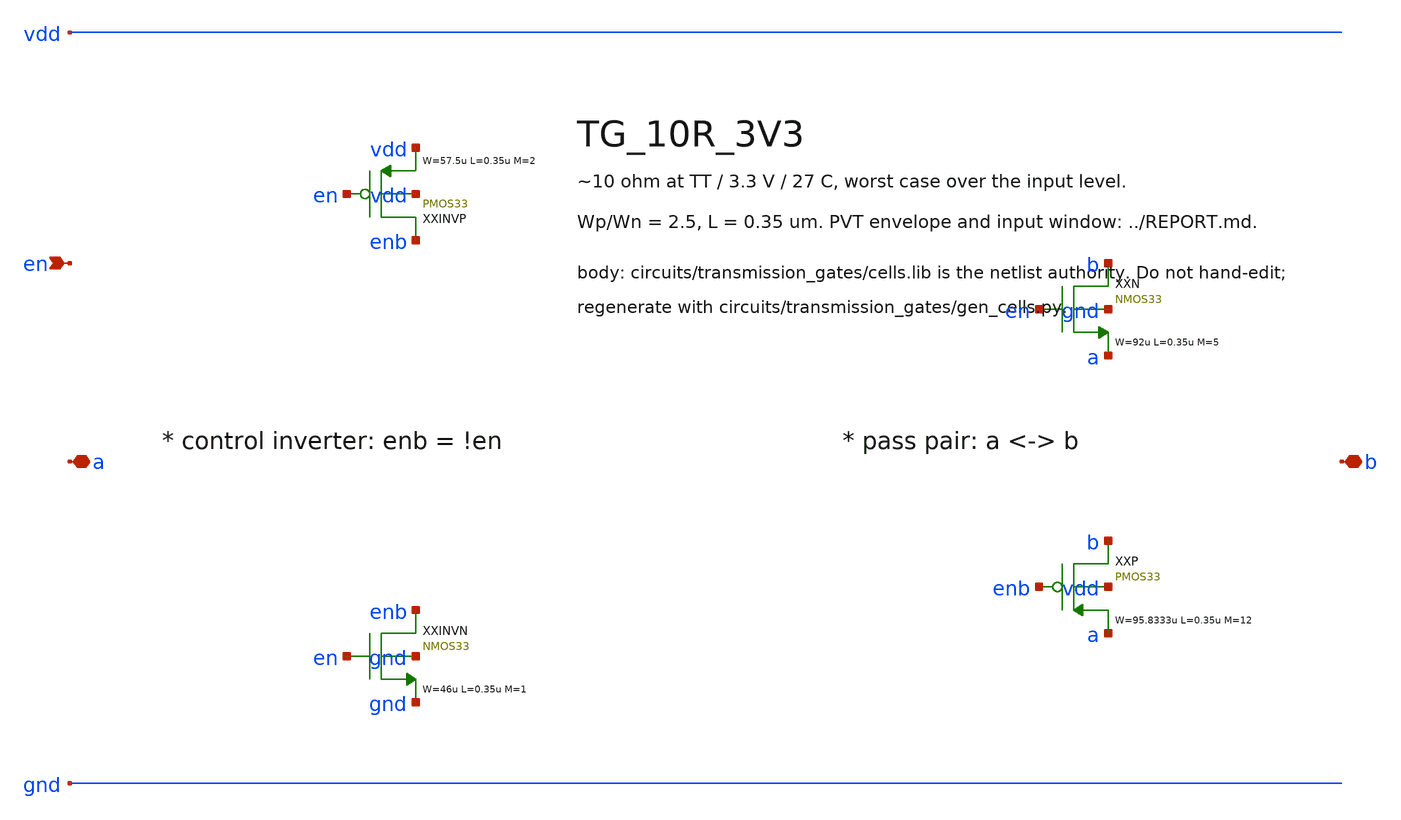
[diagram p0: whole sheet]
** sch_path: xschem/transmission_gates/TG_10R_3V3.sch
**.subckt TG_10R_3V3 a b en
*.iopin a
*.iopin b
*.ipin en
XXINVP enb en vdd vdd PMOS33 W=57.5u L=0.35u M=2 MM_SIGMA=0
XXINVN enb en gnd gnd NMOS33 W=46u L=0.35u M=1 MM_SIGMA=0
XXN b en a gnd NMOS33 W=92u L=0.35u M=5 MM_SIGMA=0
XXP b enb a vdd PMOS33 W=95.8333u L=0.35u M=12 MM_SIGMA=0
**.ends
.end
